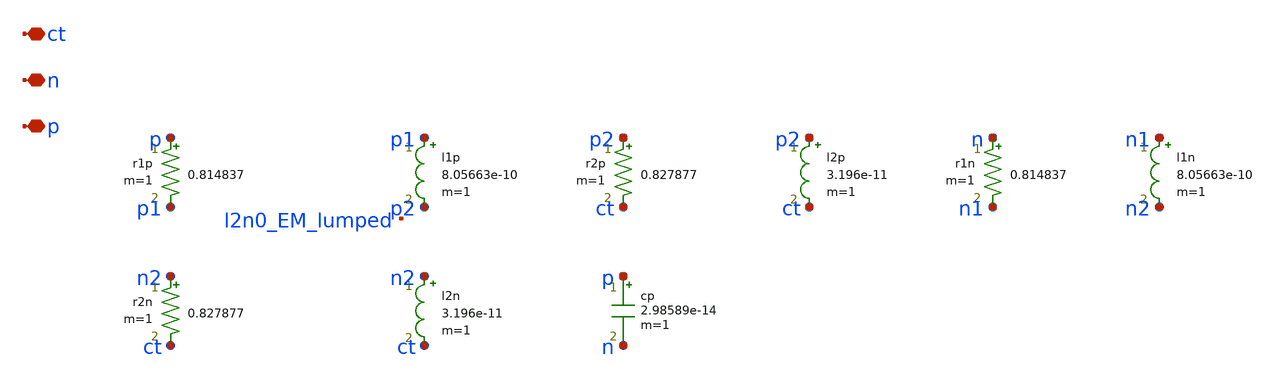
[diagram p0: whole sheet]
** sch_path: analog/vco/sch/l2n0.sch
**.subckt l2n0 p n ct
*.iopin p
*.iopin n
*.iopin ct
r1p p p1 0.814837 m=1
l1p p1 p2 8.05663e-10 m=1
r2p p2 ct 0.827877 m=1
l2p p2 ct 3.196e-11 m=1
r1n n n1 0.814837 m=1
l1n n1 n2 8.05663e-10 m=1
r2n n2 ct 0.827877 m=1
l2n n2 ct 3.196e-11 m=1
cp p n 2.98589e-14 m=1
**.ends
.end
